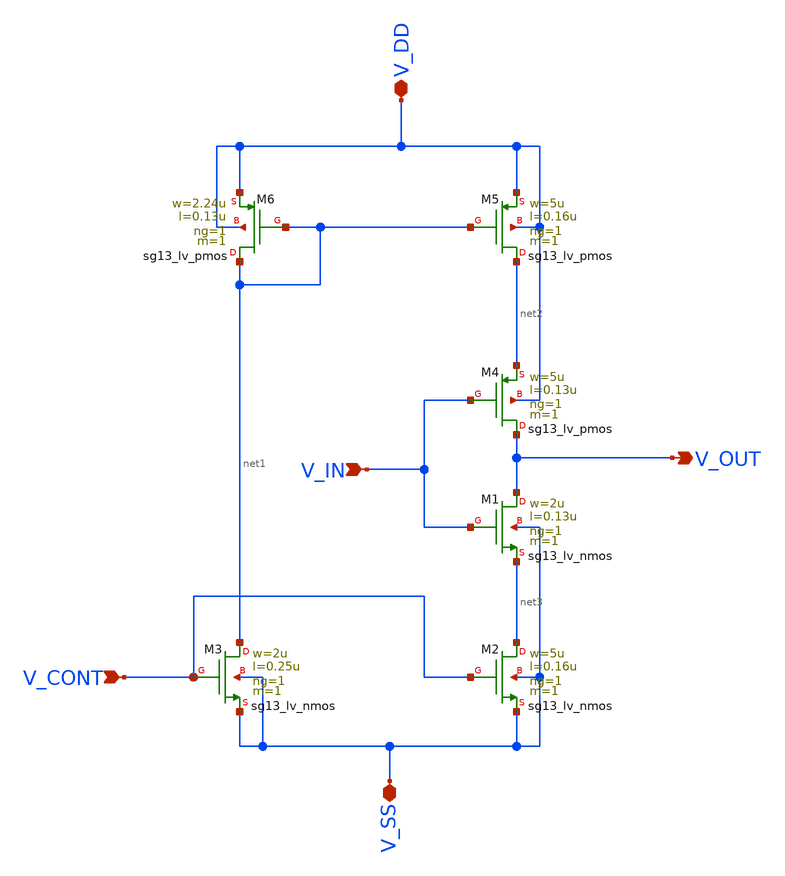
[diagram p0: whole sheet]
** sch_path: others/clemen/delay_controlable.sch
**.subckt delay_controlable V_DD V_SS V_IN V_CONT V_OUT
*.iopin V_DD
*.iopin V_SS
*.ipin V_IN
*.ipin V_CONT
*.opin V_OUT
XM1 V_OUT V_IN net3 V_SS sg13_lv_nmos w=2u l=0.13u ng=1 m=1 mm_ok=1
XM2 net3 V_CONT V_SS V_SS sg13_lv_nmos w=5u l=0.16u ng=1 m=1 mm_ok=1
XM3 net1 V_CONT V_SS V_SS sg13_lv_nmos w=2u l=0.25u ng=1 m=1 mm_ok=1
XM4 V_OUT V_IN net2 V_DD sg13_lv_pmos w=5u l=0.13u ng=1 m=1 mm_ok=1
XM5 net2 net1 V_DD V_DD sg13_lv_pmos w=5u l=0.16u ng=1 m=1 mm_ok=1
XM6 net1 net1 V_DD V_DD sg13_lv_pmos w=2.24u l=0.13u ng=1 m=1 mm_ok=1
**.ends
.end
